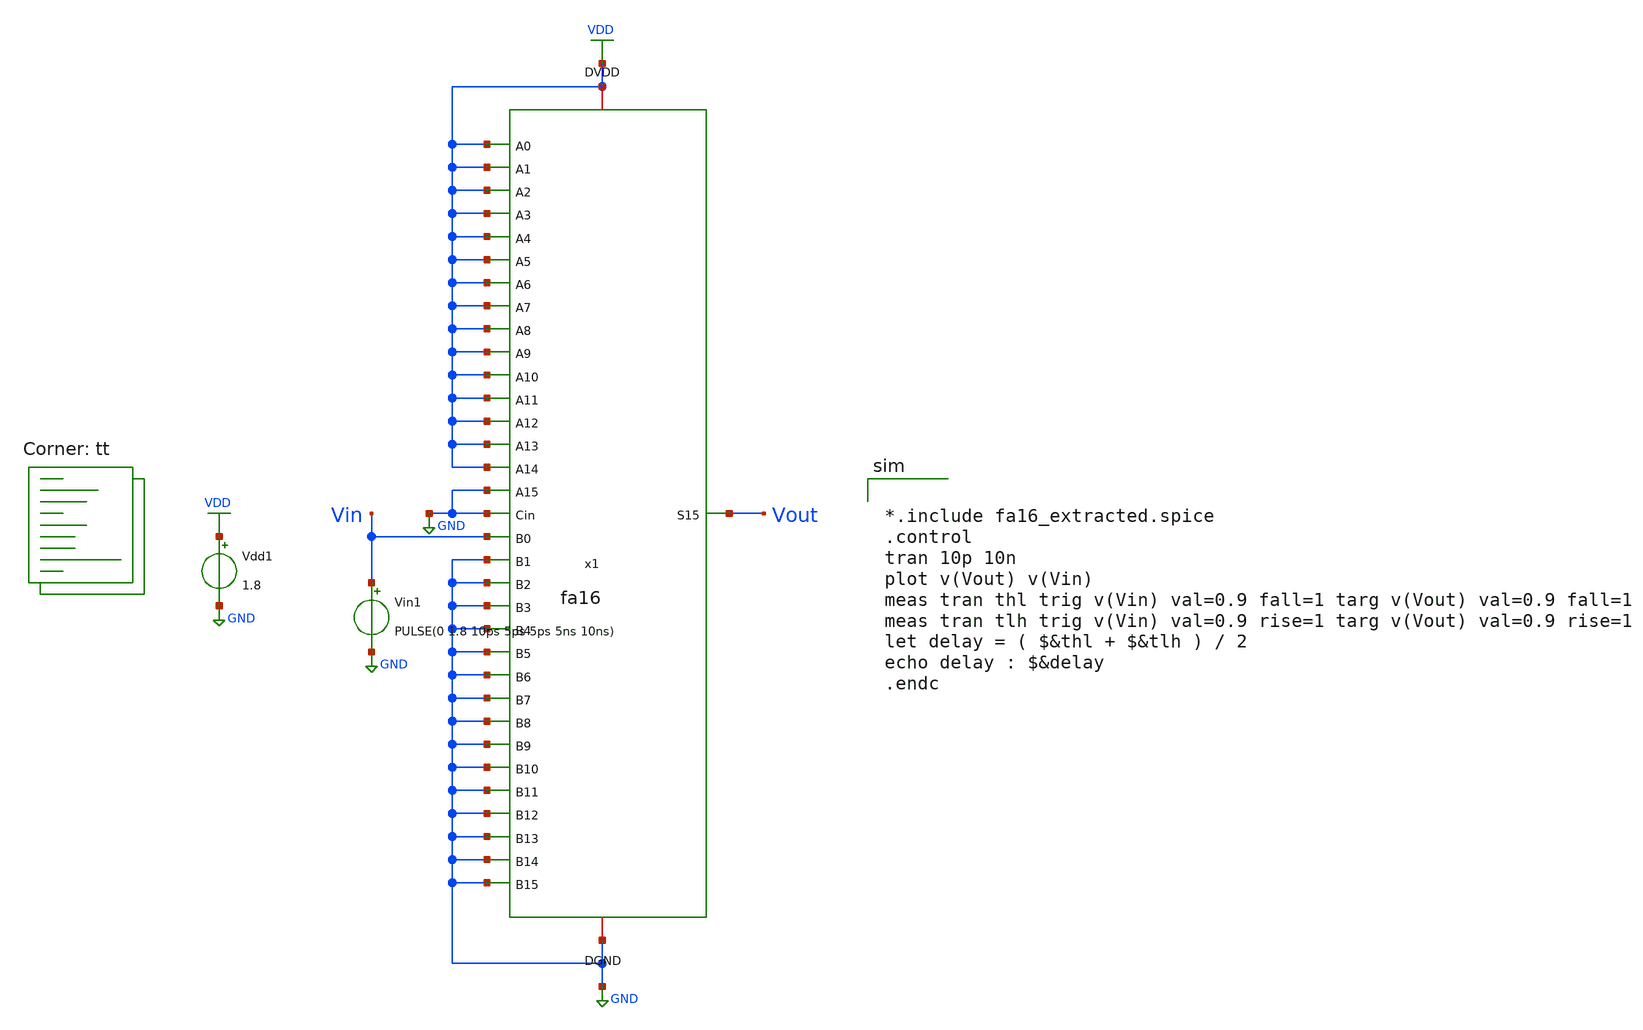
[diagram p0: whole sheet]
** sch_path: tutorial_8/fa16_test.sch
**.subckt fa16_test
x1 Vout VDD VDD VDD VDD GND VDD VDD VDD VDD GND GND VDD GND VDD VDD GND VDD VDD GND GND VDD GND GND
+ VDD VDD GND GND GND GND GND Vin GND GND GND GND fa16
Vin1 Vin GND PULSE(0 1.8 10ps 5ps 5ps 5ns 10ns)
Vdd1 VDD GND 1.8
**** begin user architecture code
.lib $::SKYWATER_MODELS/sky130.lib.spice tt


*.include fa16_extracted.spice
.control
tran 10p 10n
plot v(Vout) v(Vin)
meas tran thl trig v(Vin) val=0.9 fall=1 targ v(Vout) val=0.9 fall=1
meas tran tlh trig v(Vin) val=0.9 rise=1 targ v(Vout) val=0.9 rise=1
let delay = ( $&thl + $&tlh ) / 2
echo delay : $&delay
.endc

**** end user architecture code
**.ends
.GLOBAL GND
.GLOBAL VDD
.end
